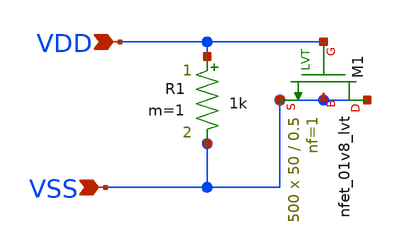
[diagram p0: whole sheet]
** sch_path: design/LELO_SVOD_SKY130A/LELO_CAP.sch
**.subckt LELO_CAP VSS VDD
*.ipin VSS
*.ipin VDD
R1 VDD VSS 1k m=1
XM1 VSS VDD VSS VSS sky130_fd_pr__nfet_01v8_lvt L=0.5 W=50 nf=1 ad='int((1 + 1)/2) * 50 / 1 * 0.29' as='int((1 + 2)/2) * 50 / 1 * 0.29'
+ pd='2*int((1 + 1)/2) * (50 / 1 + 0.29)' ps='2*int((1 + 2)/2) * (50 / 1 + 0.29)' nrd='0.29 / 50 ' nrs='0.29 / 50 '
+ sa=0 sb=0 sd=0 mult=500 m=500
**.ends
.end
